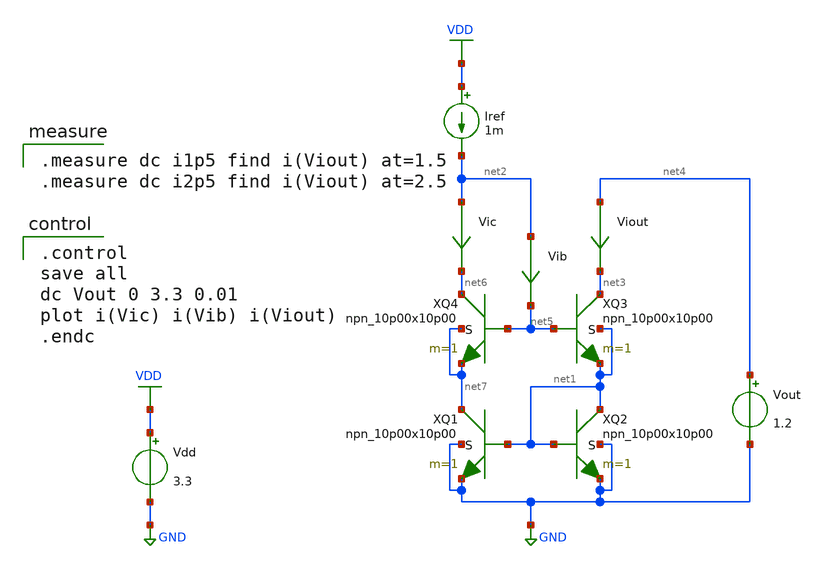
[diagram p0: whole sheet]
** sch_path: current-source/cm-wilson2-bjt.sch
**.subckt cm-wilson2-bjt
XQ2 net1 net1 GND GND npn_10p00x10p00 m=1
XQ1 net7 net1 GND GND npn_10p00x10p00 m=1
Viout net4 net3 0
.save i(viout)
Vdd VDD GND 3.3
Iref VDD net2 1m
Vic net2 net6 0
.save i(vic)
Vib net2 net5 0
.save i(vib)
Vout net4 GND 1.2
XQ3 net3 net5 net1 net1 npn_10p00x10p00 m=1
XQ4 net6 net5 net7 net7 npn_10p00x10p00 m=1
**** begin user architecture code

.include $::180MCU_MODELS/design.ngspice
.lib $::180MCU_MODELS/sm141064.ngspice typical
.lib $::180MCU_MODELS/sm141064.ngspice res_typical
.lib $::180MCU_MODELS/sm141064.ngspice moscap_typical
.lib $::180MCU_MODELS/sm141064.ngspice bjt_typical
* .lib $::180MCU_MODELS/sm141064.ngspice res_statistical


.control
save all
dc Vout 0 3.3 0.01
plot i(Vic) i(Vib) i(Viout)
.endc


.measure dc i1p5 find i(Viout) at=1.5
.measure dc i2p5 find i(Viout) at=2.5

**** end user architecture code
**.ends
.GLOBAL GND
.GLOBAL VDD
.end
